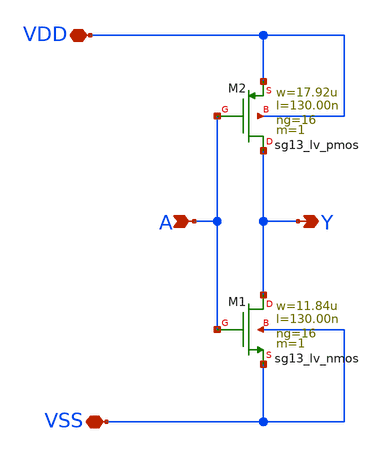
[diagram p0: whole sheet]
** sch_path: ihp-sg13g2/libs.tech/xschem/sg13g2_stdcells/sg13g2_inv_16.sch
**.subckt sg13g2_inv_16 Y VSS A VDD
*.opin Y
*.iopin VSS
*.ipin A
*.iopin VDD
XM1 Y A VSS VSS sg13_lv_nmos w=11.84u l=130.00n ng=16 m=1 mm_ok=1
XM2 Y A VDD VDD sg13_lv_pmos w=17.92u l=130.00n ng=16 m=1 mm_ok=1
**.ends
.end
